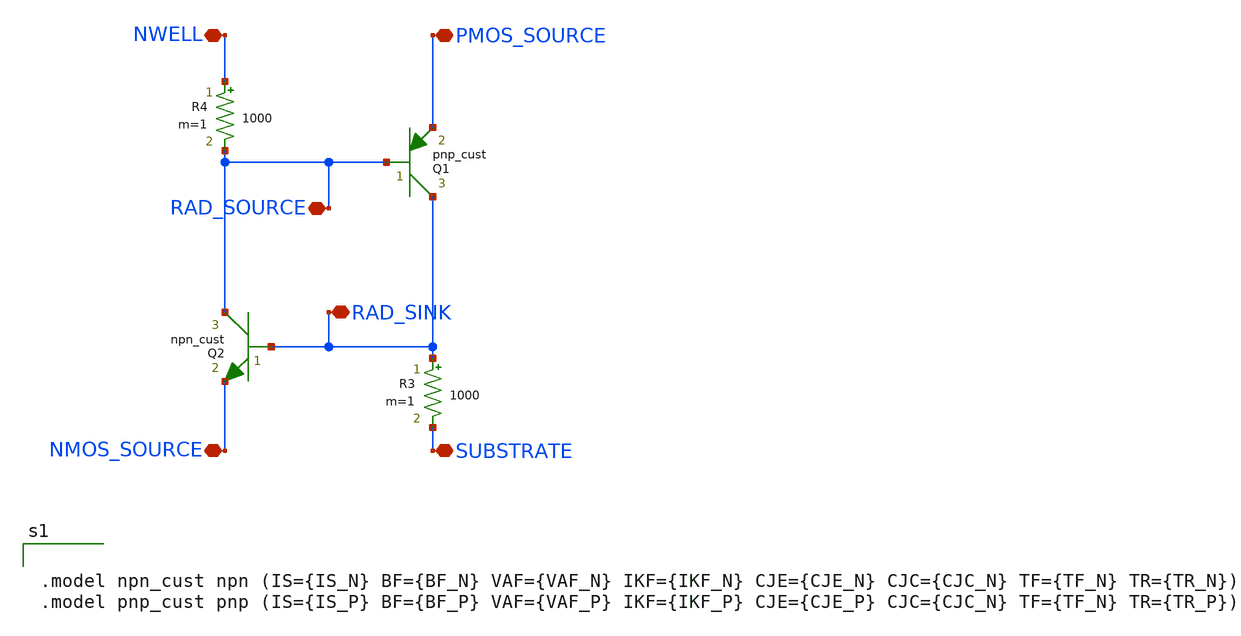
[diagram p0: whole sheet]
** sch_path: latchup/basic_model.sch
**.subckt basic_model NWELL SUBSTRATE RAD_SOURCE RAD_SINK NMOS_SOURCE PMOS_SOURCE
*.iopin NWELL
*.iopin SUBSTRATE
*.iopin RAD_SOURCE
*.iopin RAD_SINK
*.iopin NMOS_SOURCE
*.iopin PMOS_SOURCE
Q1 RAD_SINK RAD_SOURCE PMOS_SOURCE pnp_cust area=1 m=1
Q2 RAD_SOURCE RAD_SINK NMOS_SOURCE npn_cust area=1 m=1
R3 RAD_SINK SUBSTRATE 1000 m=1
R4 NWELL RAD_SOURCE 1000 m=1
**** begin user architecture code


.model npn_cust npn (IS={IS_N} BF={BF_N} VAF={VAF_N} IKF={IKF_N} CJE={CJE_N} CJC={CJC_N} TF={TF_N} TR={TR_N})
.model pnp_cust pnp (IS={IS_P} BF={BF_P} VAF={VAF_P} IKF={IKF_P} CJE={CJE_P} CJC={CJC_N} TF={TF_N} TR={TR_P})


**** end user architecture code
**.ends
.end
